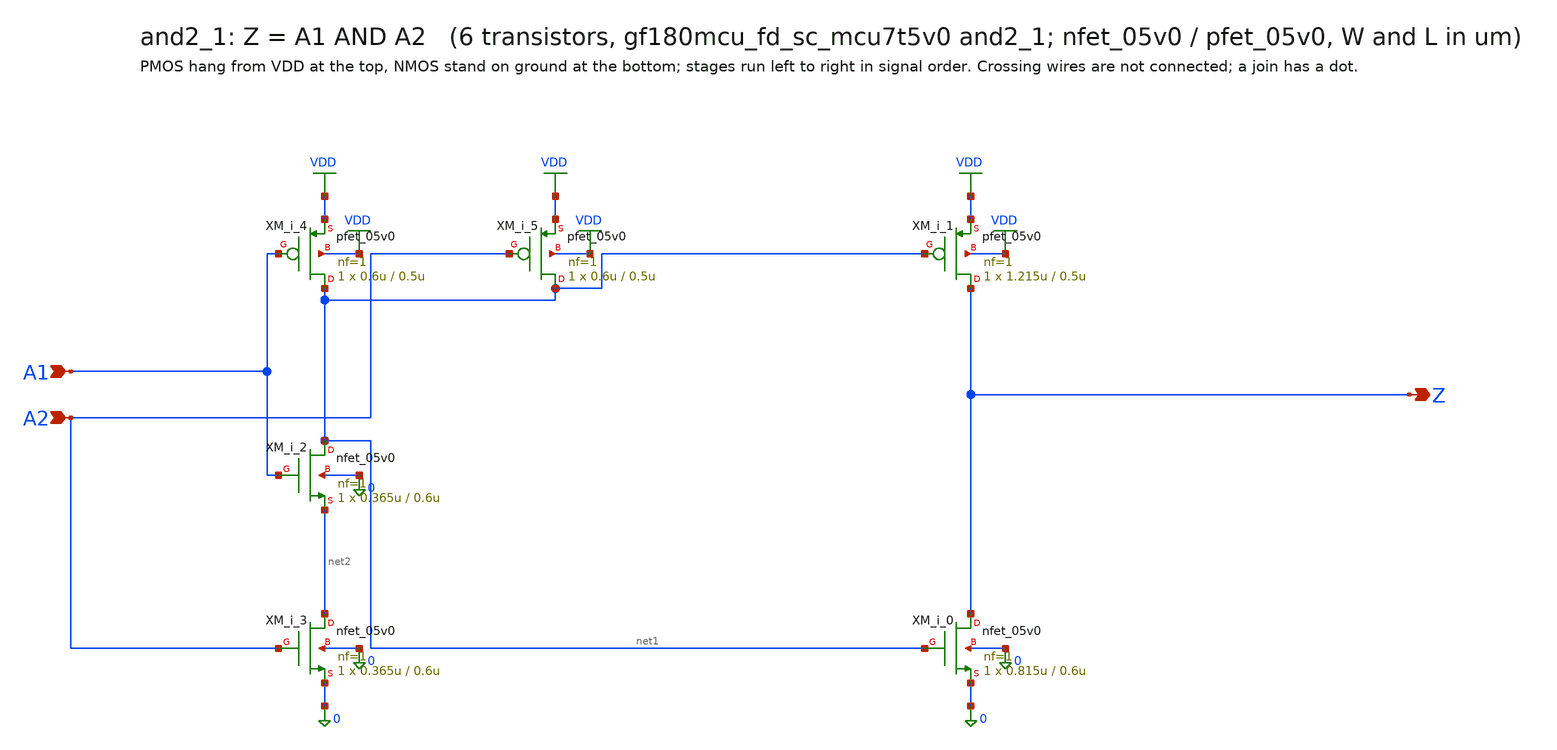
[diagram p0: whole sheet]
** sch_path: xschem/cells_tx/and2_1.sch
**.subckt and2_1 A1 A2 Z
*.ipin A1
*.ipin A2
*.opin Z
XM_i_2 net1 A1 net2 0 nfet_05v0 L=0.6u W=0.365u nf=1 ad=1.825e-13 as=1.825e-13 pd=1.73e-06
+ ps=1.73e-06 nrd=0 nrs=0 sa=0 sb=0 sd=0 m=1
XM_i_3 net2 A2 0 0 nfet_05v0 L=0.6u W=0.365u nf=1 ad=1.825e-13 as=1.825e-13 pd=1.73e-06 ps=1.73e-06
+ nrd=0 nrs=0 sa=0 sb=0 sd=0 m=1
XM_i_0 Z net1 0 0 nfet_05v0 L=0.6u W=0.815u nf=1 ad=4.075e-13 as=4.075e-13 pd=2.63e-06 ps=2.63e-06
+ nrd=0 nrs=0 sa=0 sb=0 sd=0 m=1
XM_i_4 net1 A1 VDD VDD pfet_05v0 L=0.5u W=0.6u nf=1 ad=3e-13 as=3e-13 pd=2.2e-06 ps=2.2e-06 nrd=0
+ nrs=0 sa=0 sb=0 sd=0 m=1
XM_i_5 net1 A2 VDD VDD pfet_05v0 L=0.5u W=0.6u nf=1 ad=3e-13 as=3e-13 pd=2.2e-06 ps=2.2e-06 nrd=0
+ nrs=0 sa=0 sb=0 sd=0 m=1
XM_i_1 Z net1 VDD VDD pfet_05v0 L=0.5u W=1.215u nf=1 ad=6.075e-13 as=6.075e-13 pd=3.43e-06
+ ps=3.43e-06 nrd=0 nrs=0 sa=0 sb=0 sd=0 m=1
**.ends
.GLOBAL VDD
.end
